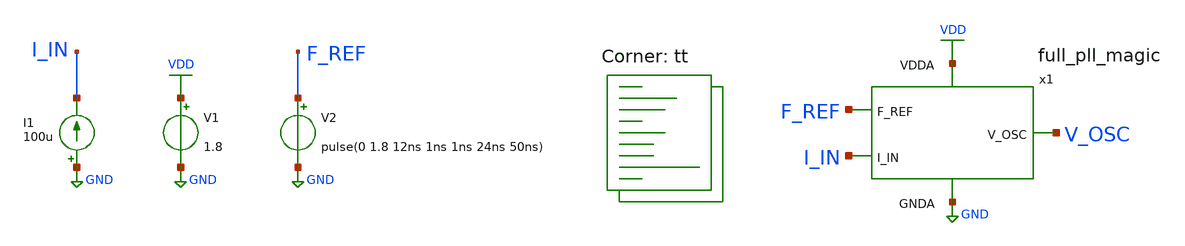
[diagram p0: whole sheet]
** sch_path: projects/pll/full_pll/magic/tb_full_pll_magic.sch
**.subckt tb_full_pll_magic
V1 VDD GND 1.8
V2 F_REF GND pulse(0 1.8 12ns 1ns 1ns 24ns 50ns)
I1 GND I_IN 100u
x1 V_OSC VDD GND F_REF I_IN full_pll_magic
**** begin user architecture code
.lib $::SKYWATER_MODELS/sky130.lib.spice tt



.include /foss/designs/my_design/projects/pll/full_pll/magic/full_pll_magic.spice

.option method=gear
* .option method=trap
.option wnflag=1
* .option savecurrents

.save v(x1.v_cont.n0) v(x1.f_vco.t0) v(x1.pfd_8_0.qa.n0) v(x1.pfd_8_0.qb.n0) v(x1.pfd_8_0.up_input.n0) v(x1.pfd_8_0.down_input.n0) v(x1.charge_pump_cell_6_0.x.n0) v(x1.vco_fd_magic_0.div120_2_0.div2.n0) v(x1.vco_fd_magic_0.div120_2_0.div4.n0) v(x1.vco_fd_magic_0.div120_2_0.div8.n0) v(x1.vco_fd_magic_0.div120_2_0.div24.n0) @m.x1.x39.msky130_fd_pr__pfet_01v8[id] @m.x1.x70.msky130_fd_pr__pfet_01v8[id] @m.x1.x101.msky130_fd_pr__pfet_01v8[id] @m.x1.x124.msky130_fd_pr__pfet_01v8[id] @m.x1.x213.msky130_fd_pr__nfet_01v8[id] @m.x1.x241.msky130_fd_pr__nfet_01v8[id]


* V_out initial voltage

.ic v(x1.v_cont.n0) = 0.0


.control
  save v(v_osc)

  * timestep for exact simulation results
  tran 5ps 6us

  remzerovec
  write tb_full_pll_magic_4.raw
  wrdata /foss/designs/my_design/projects/pll/full_pll/magic/full_pll_v_osc.txt v(v_osc)
  set appendwrite

.endc



**** end user architecture code
**.ends
.GLOBAL GND
.GLOBAL VDD
.end
